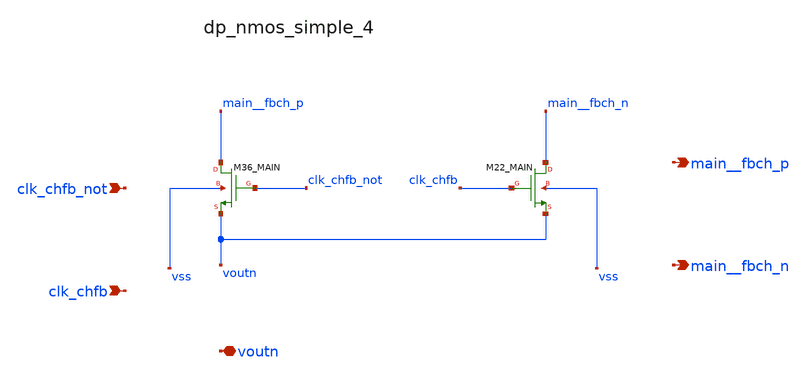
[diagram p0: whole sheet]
** sch_path: analog-db/raw/ia_004_fan_chopper_rrl/hier/blocks/dp_nmos_simple_4.sch
**.subckt dp_nmos_simple_4 clk_chfb_not clk_chfb voutn main__fbch_p main__fbch_n
*.ipin clk_chfb_not
*.ipin clk_chfb
*.iopin voutn
*.opin main__fbch_p
*.opin main__fbch_n
XM22_MAIN main__fbch_n clk_chfb voutn vss sg13_lv_nmos w=x_dut_xm22_main_w l=x_dut_xm22_main_l ng=1
+ m=x_dut_xm22_main_m
XM36_MAIN main__fbch_p clk_chfb_not voutn vss sg13_lv_nmos w=x_dut_xm36_main_w l=x_dut_xm36_main_l
+ ng=1 m=x_dut_xm36_main_m
**.ends
.end
